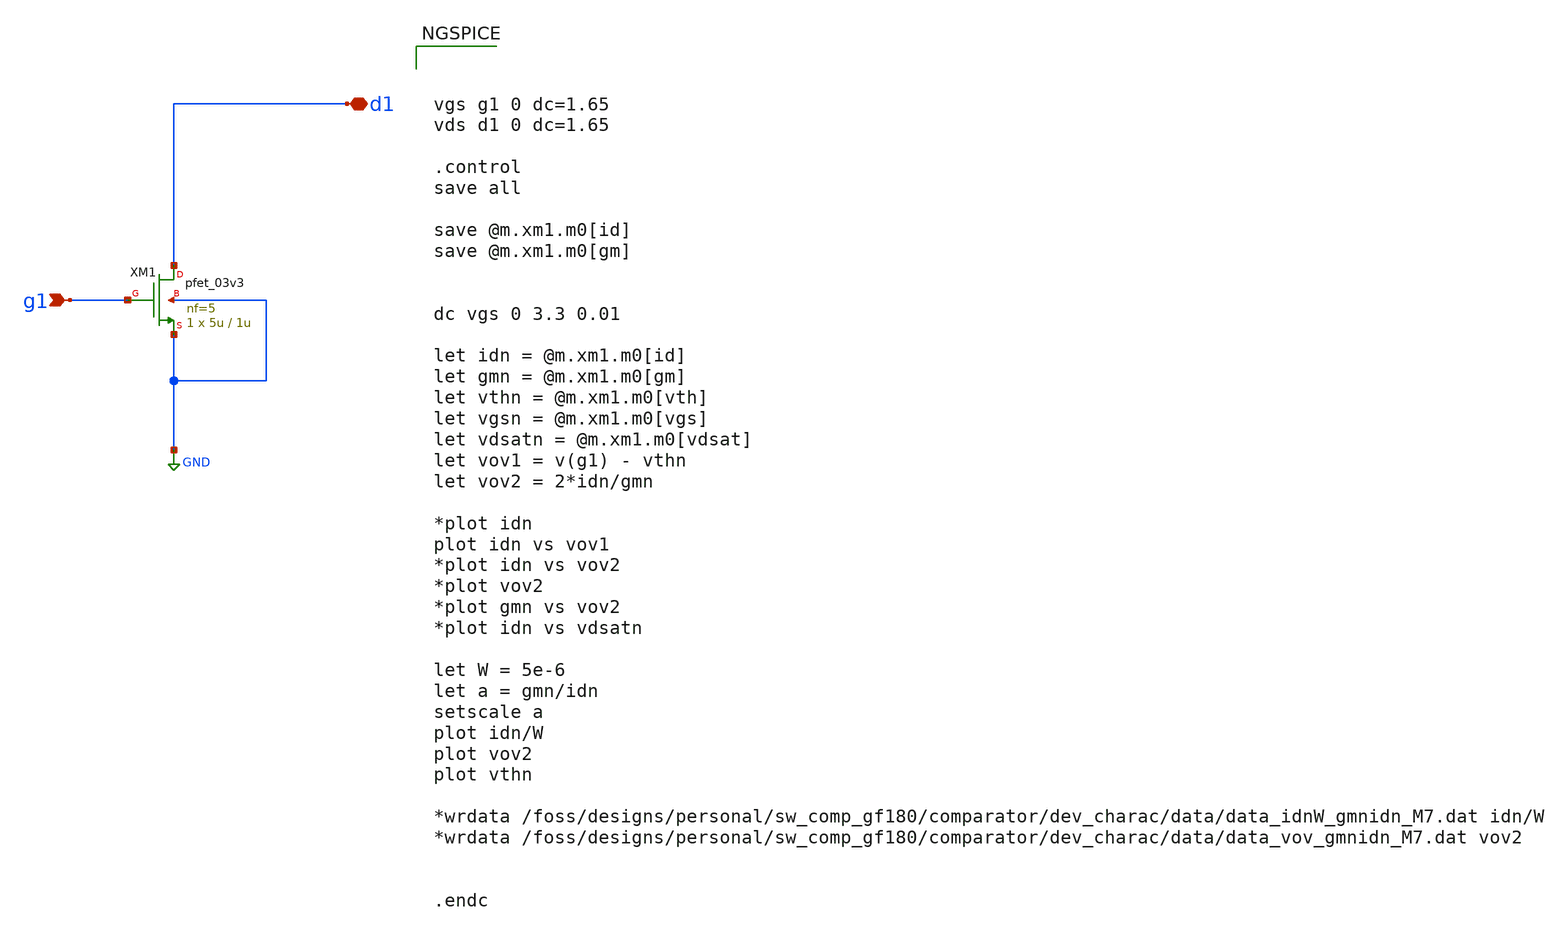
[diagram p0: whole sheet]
** sch_path: xschem/test/dev_charac/nmos_charac_gf180_3p3_M7.sch

.include $env(PDK_ROOT)/$env(PDK)/libs.tech/ngspice/design.ngspice

.lib $env(PDK_ROOT)/$env(PDK)/libs.tech/ngspice/sm141064.ngspice typical
.lib $env(PDK_ROOT)/$env(PDK)/libs.tech/ngspice/sm141064.ngspice mimcap_statistical
.lib $env(PDK_ROOT)/$env(PDK)/libs.tech/ngspice/sm141064.ngspice cap_mim
.lib $env(PDK_ROOT)/$env(PDK)/libs.tech/ngspice/sm141064.ngspice res_typical
.lib $env(PDK_ROOT)/$env(PDK)/libs.tech/ngspice/sm141064.ngspice bjt_typical
.lib $env(PDK_ROOT)/$env(PDK)/libs.tech/ngspice/sm141064.ngspice moscap_typical


**.subckt nmos_charac_gf180_3p3_M7 g1 d1
*.ipin g1
*.iopin d1
XM1 d1 g1 GND GND pfet_03v3 L=1u W=5u nf=5 ad='int((nf+1)/2) * W/nf * 0.18u' as='int((nf+2)/2) * W/nf * 0.18u'
+ pd='2*int((nf+1)/2) * (W/nf + 0.18u)' ps='2*int((nf+2)/2) * (W/nf + 0.18u)' nrd='0.18u / W' nrs='0.18u / W'
+ sa=0 sb=0 sd=0 m=1
**** begin user architecture code



vgs g1 0 dc=1.65
vds d1 0 dc=1.65

.control
save all

save @m.xm1.m0[id]
save @m.xm1.m0[gm]


dc vgs 0 3.3 0.01

let idn = @m.xm1.m0[id]
let gmn = @m.xm1.m0[gm]
let vthn = @m.xm1.m0[vth]
let vgsn = @m.xm1.m0[vgs]
let vdsatn = @m.xm1.m0[vdsat]
let vov1 = v(g1) - vthn
let vov2 = 2*idn/gmn

*plot idn
plot idn vs vov1
*plot idn vs vov2
*plot vov2
*plot gmn vs vov2
*plot idn vs vdsatn

let W = 5e-6
let a = gmn/idn
setscale a
plot idn/W
plot vov2
plot vthn

*wrdata /foss/designs/personal/sw_comp_gf180/comparator/dev_charac/data/data_idnW_gmnidn_M7.dat
*+ idn/W
*wrdata /foss/designs/personal/sw_comp_gf180/comparator/dev_charac/data/data_vov_gmnidn_M7.dat vov2


.endc


**** end user architecture code
**.ends
.GLOBAL GND
.end
